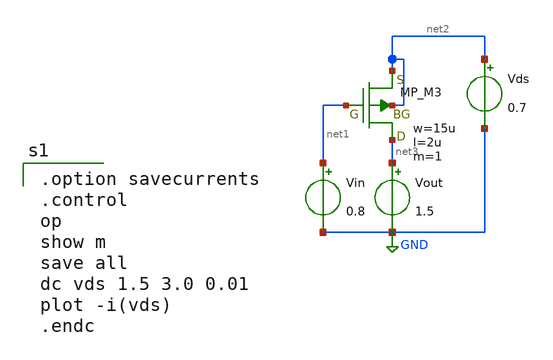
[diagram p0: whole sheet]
** sch_path: member_project/DCDC/xschem/pmos_id_diff.sch
**.subckt pmos_id_diff
XM3 net3 net1 net2 net2 PMOS w=15u l=2u as=0 ad=0 ps=0 pd=0 nrd=0 nrs=0 m=1
Vds net2 GND 0.7
Vin net1 GND 0.8
Vout net3 GND 1.5
**** begin user architecture code
 .include $::LIB/ip62_models

.option savecurrents
.control
op
show m
save all
dc vds 1.5 3.0 0.01
plot -i(vds)
.endc

**** end user architecture code
**.ends
.GLOBAL GND
.end
